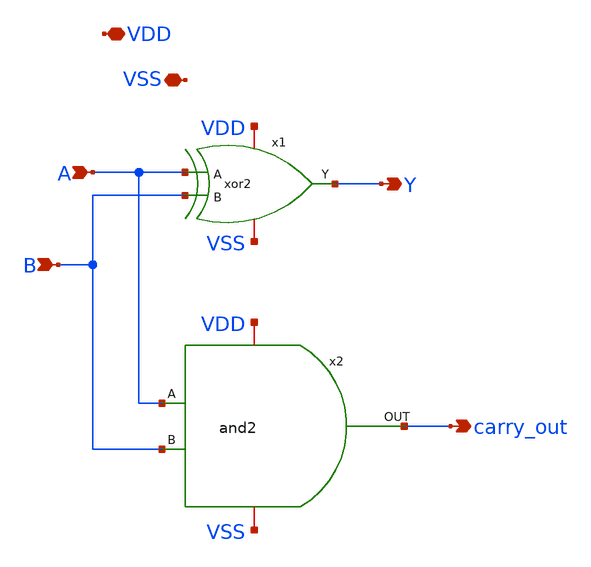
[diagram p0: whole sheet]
** sch_path: design/ARITMETIC_UNIT/xschem/half_adder.sch
**.subckt half_adder A B Y carry_out VDD VSS
*.ipin A
*.ipin B
*.opin Y
*.opin carry_out
*.iopin VDD
*.iopin VSS
x1 Y A VDD VSS B xor2
x2 VSS A B VDD carry_out and2
**.ends
.end
